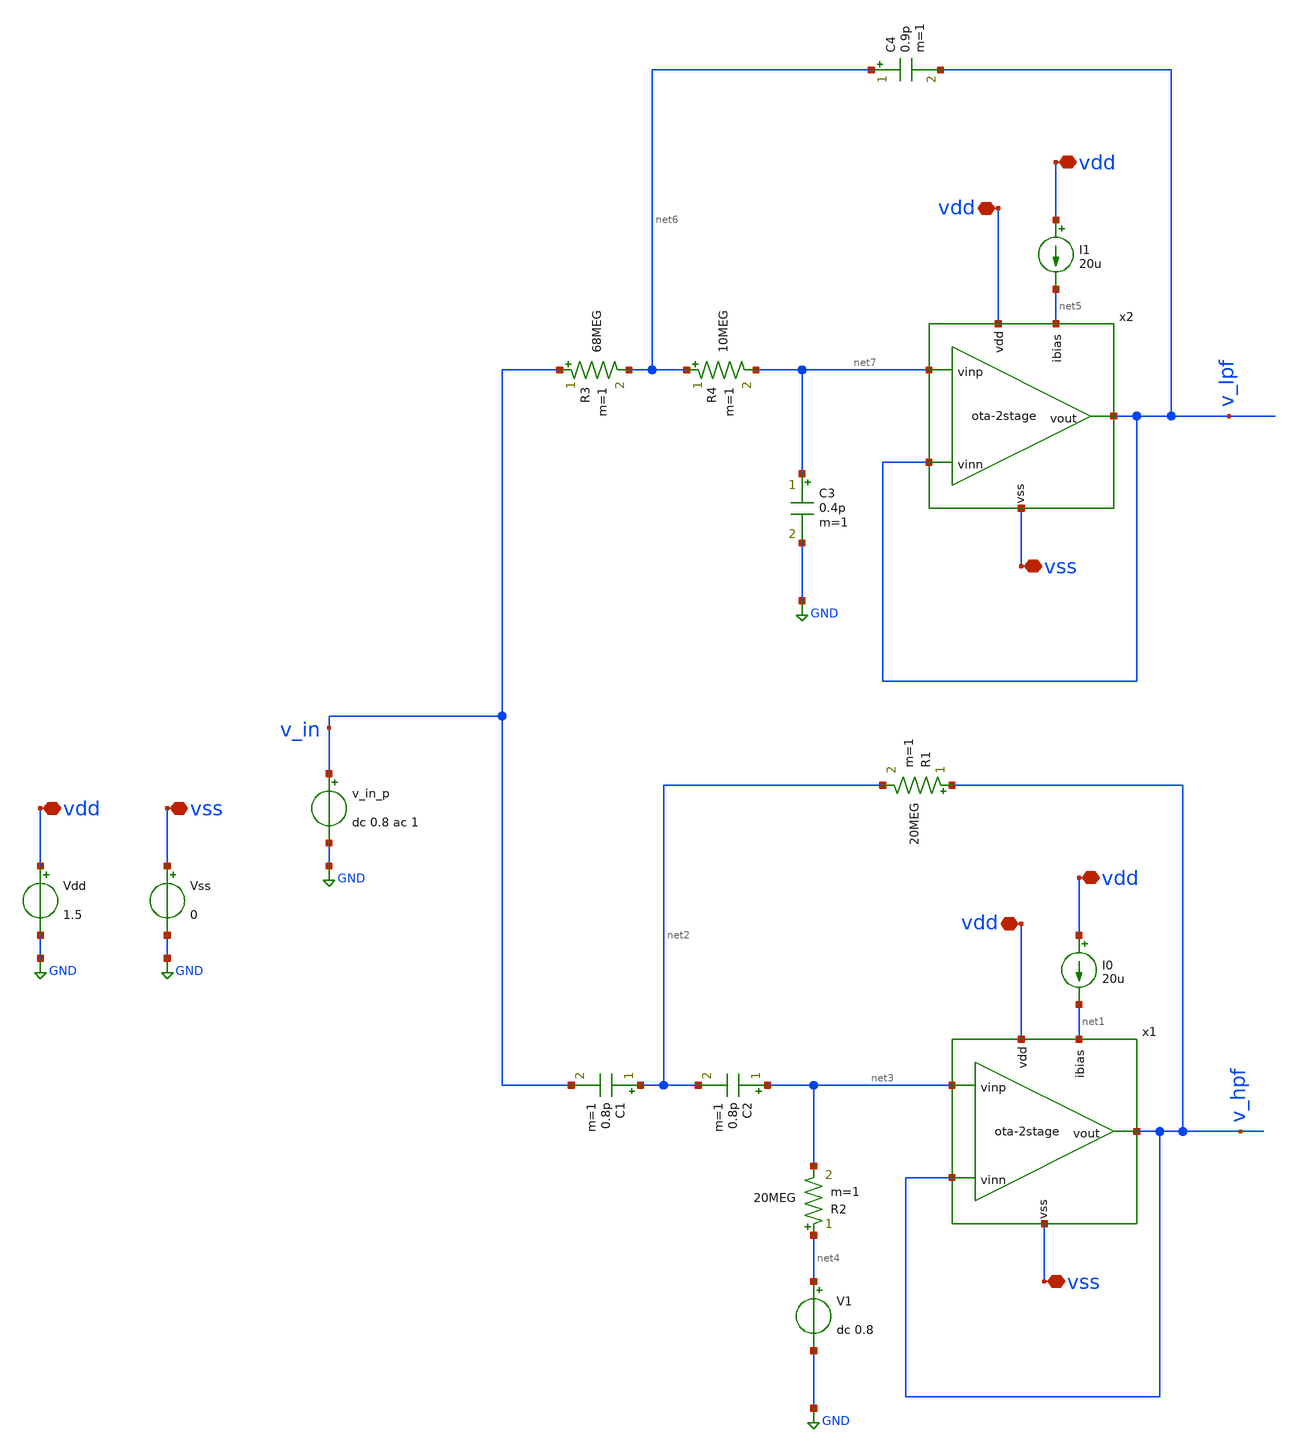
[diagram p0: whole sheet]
** sch_path: xschem/ota-2stage_tb-sk-LR2.sch
**.subckt ota-2stage_tb-sk-LR2 vdd vdd vdd vss vss vdd vdd vss
*.iopin vdd
*.iopin vdd
*.iopin vdd
*.iopin vss
*.iopin vss
*.iopin vdd
*.iopin vdd
*.iopin vss
I0 vdd net1 20u
Vdd vdd GND 1.5
Vss vss GND 0
v_in_p v_in GND dc 0.8 ac 1
x1 vdd net1 v_hpf v_hpf net3 vss ota-2stage
R1 v_hpf net2 20MEG m=1
R2 net4 net3 20MEG m=1
C1 net2 v_in 0.8p m=1
C2 net3 net2 0.8p m=1
V1 net4 GND dc 0.8
I1 vdd net5 20u
R3 v_in net6 68MEG m=1
R4 net6 net7 10MEG m=1
C3 net7 GND 0.4p m=1
C4 net6 v_lpf 0.9p m=1
x2 vdd net5 v_lpf v_lpf net7 vss ota-2stage
**** begin user architecture code
 .lib cornerMOSlv.lib mos_tt
.lib cornerCAP.lib cap_typ
.lib cornerRES.lib res_typ



.temp 27
.control
option sparse
save all

* Sweep from 100 Hz to 1 MHz
ac dec 101 100 1MEG

* Plot the response to see 10kHz cutoff
let LPF = 20*log10(v(v_lpf))
let HPF = 20*log10(v(v_hpf))
let SUM = 20*log10(mag(v(v_lpf) + v(v_hpf)))
let DIF = 20*log10(mag(v(v_lpf) - v(v_hpf)))
plot LPF HPF SUM DIF title 'Frequency Responce'

let LPF_PHASE = vp(v_lpf)
let HPF_PHASE = vp(v_hpf)
plot LPF_PHASE HPF_PHASE title 'Phase Responce'

* Measure the exact maximum DC gain of the Low-Pass section
meas ac max_gain MAX vmag(v_lpf) FROM=100 TO=1k

* For LR4, the crossover target is exactly half the voltage amplitude (-6dB)
let fc_target = max_gain / 2

* Find the exact frequency where the LPF drops to that target (-6dB)
meas ac crossover_freq WHEN vmag(v_lpf)=fc_target FALL=1

* 1. Find the voltage magnitudes at 100kHz and 1MHz
meas ac v_lpf_100k FIND vmag(v_lpf) AT=100k
meas ac v_lpf_1meg FIND vmag(v_lpf) AT=1MEG

* 2. Convert both points to dB and subtract to find the drop per decade
let db_lpf_100k = 20 * log10(v_lpf_100k)
let db_lpf_1meg = 20 * log10(v_lpf_1meg)
let slope_lpf = db_lpf_1meg - db_lpf_100k

* 1. Find the voltage magnitudes at 100Hz and 1kHz
meas ac v_hpf_100 FIND vmag(v_hpf) AT=100
meas ac v_hpf_1k   FIND vmag(v_hpf) AT=1k

* 2. Convert both points to dB and subtract to find the rise per decade
let db_hpf_100 = 20 * log10(v_hpf_100)
let db_hpf_1k   = 20 * log10(v_hpf_1k)
let slope_hpf = db_hpf_1k - db_hpf_100

print max_gain
print crossover_freq
print slope_lpf
print slope_hpf

.endc


**** end user architecture code
**.ends
.GLOBAL GND
.end
